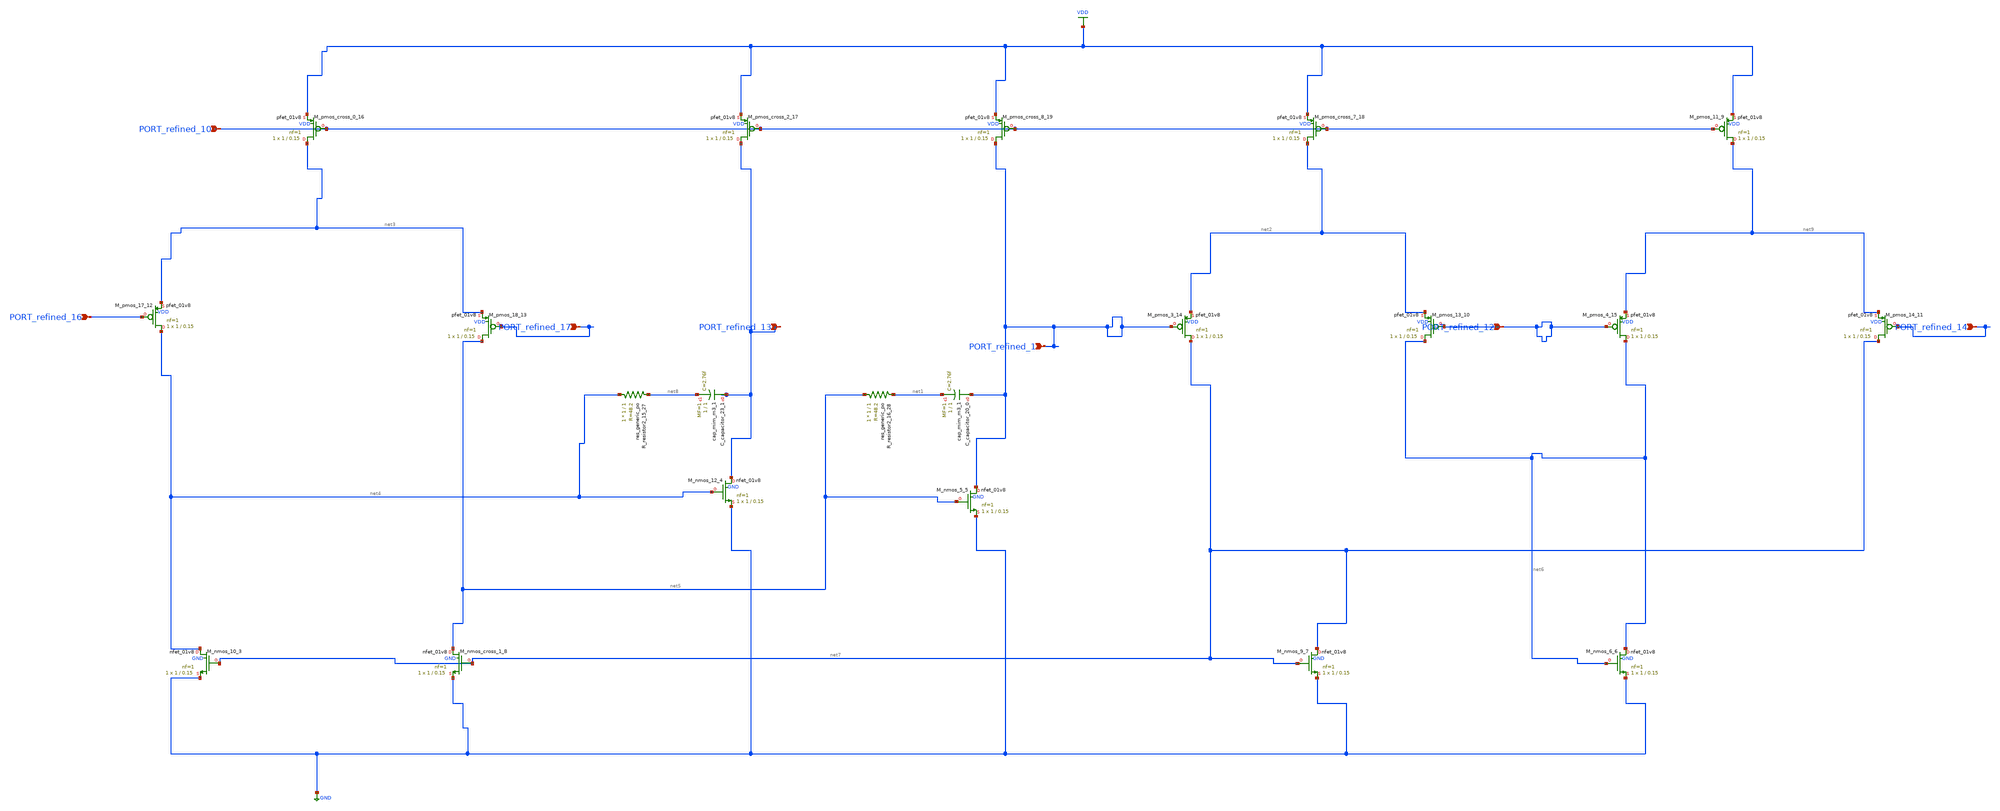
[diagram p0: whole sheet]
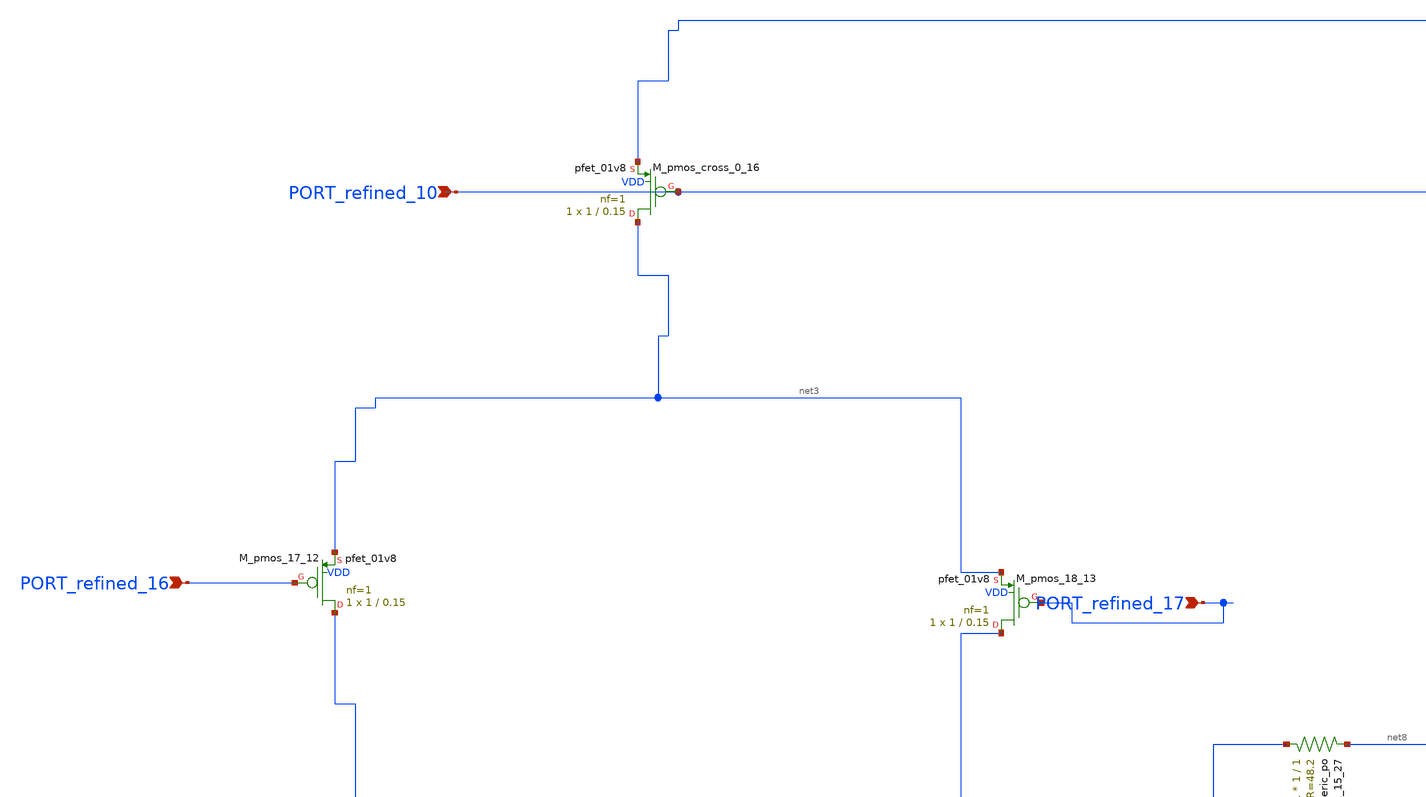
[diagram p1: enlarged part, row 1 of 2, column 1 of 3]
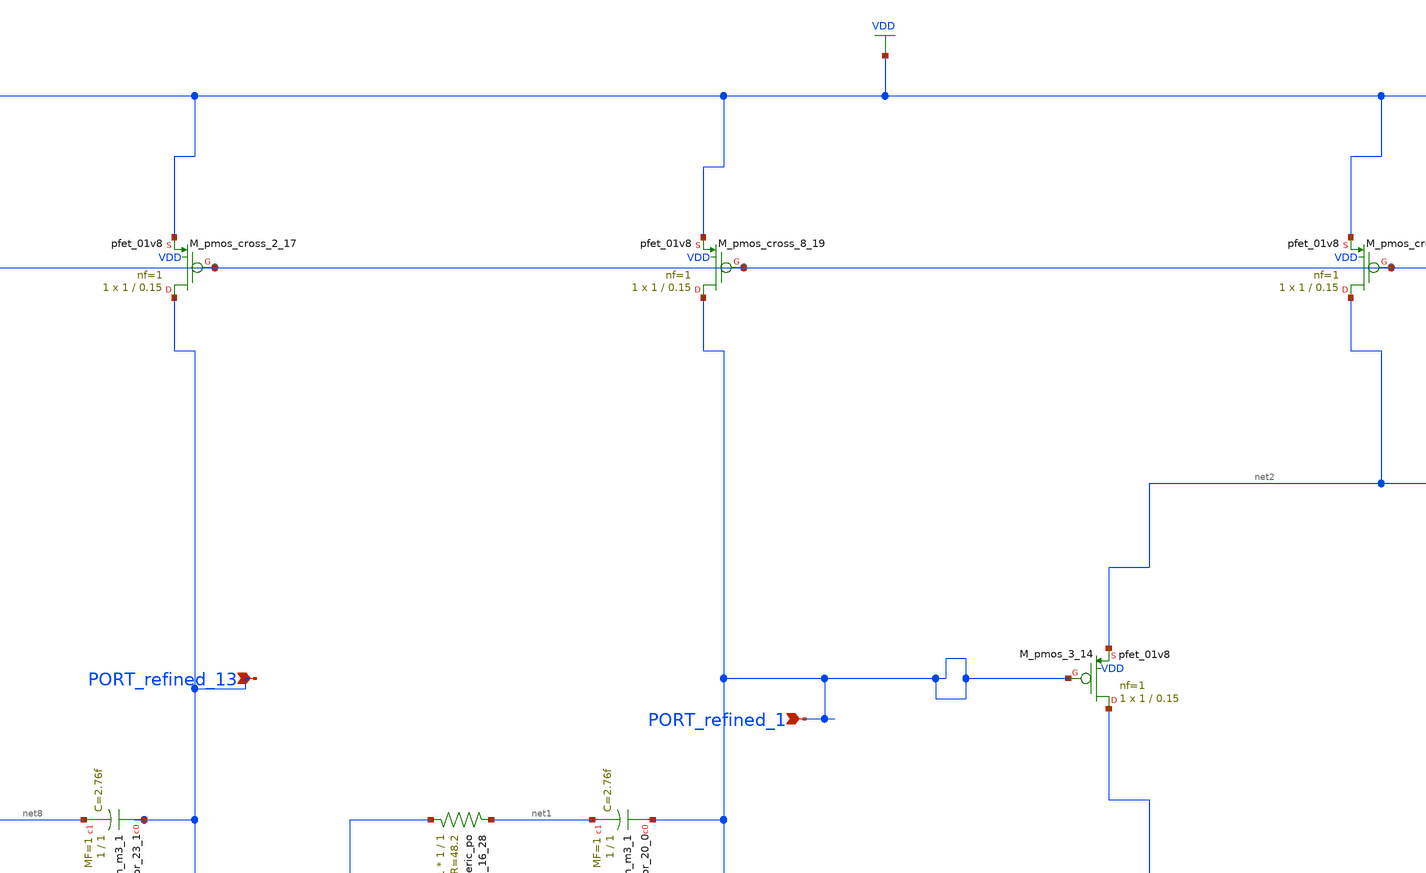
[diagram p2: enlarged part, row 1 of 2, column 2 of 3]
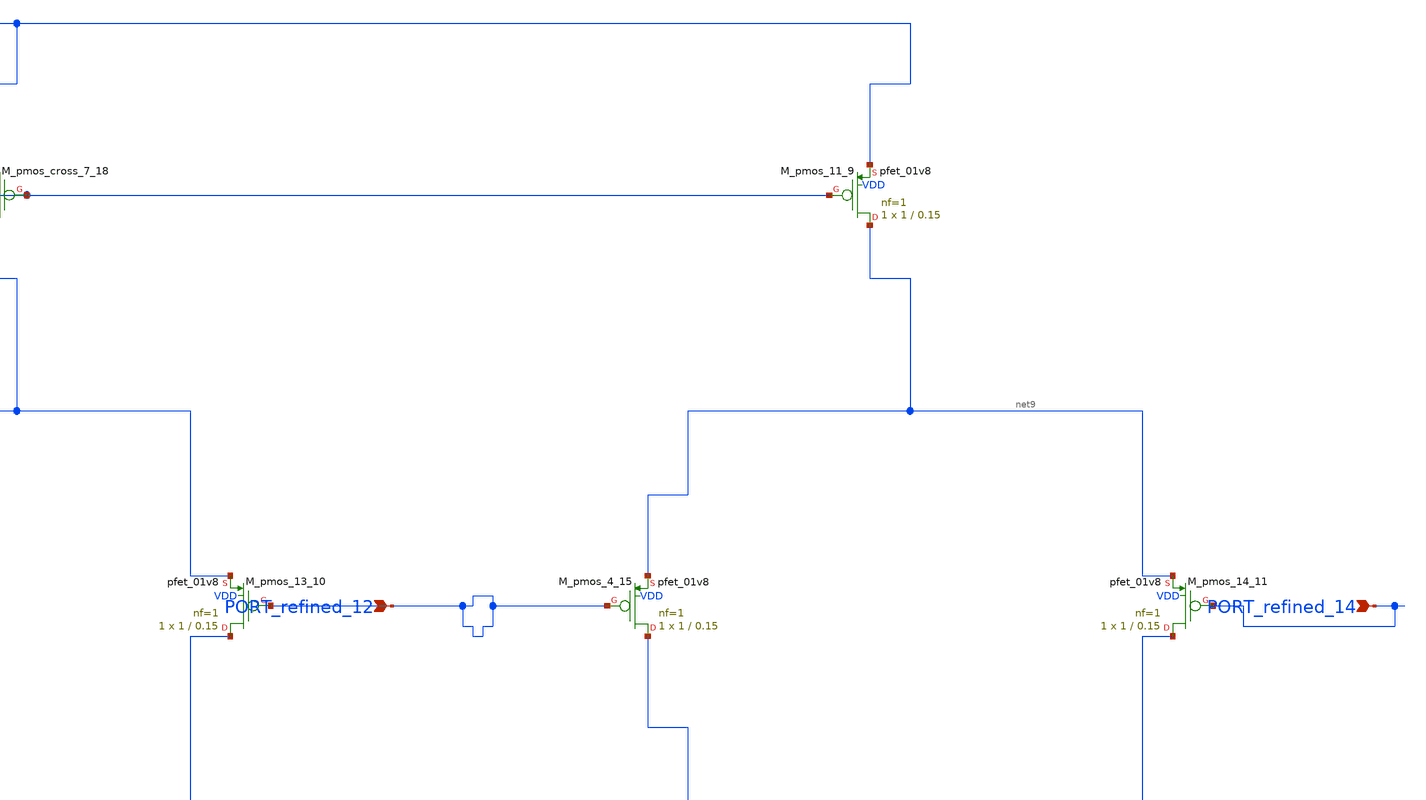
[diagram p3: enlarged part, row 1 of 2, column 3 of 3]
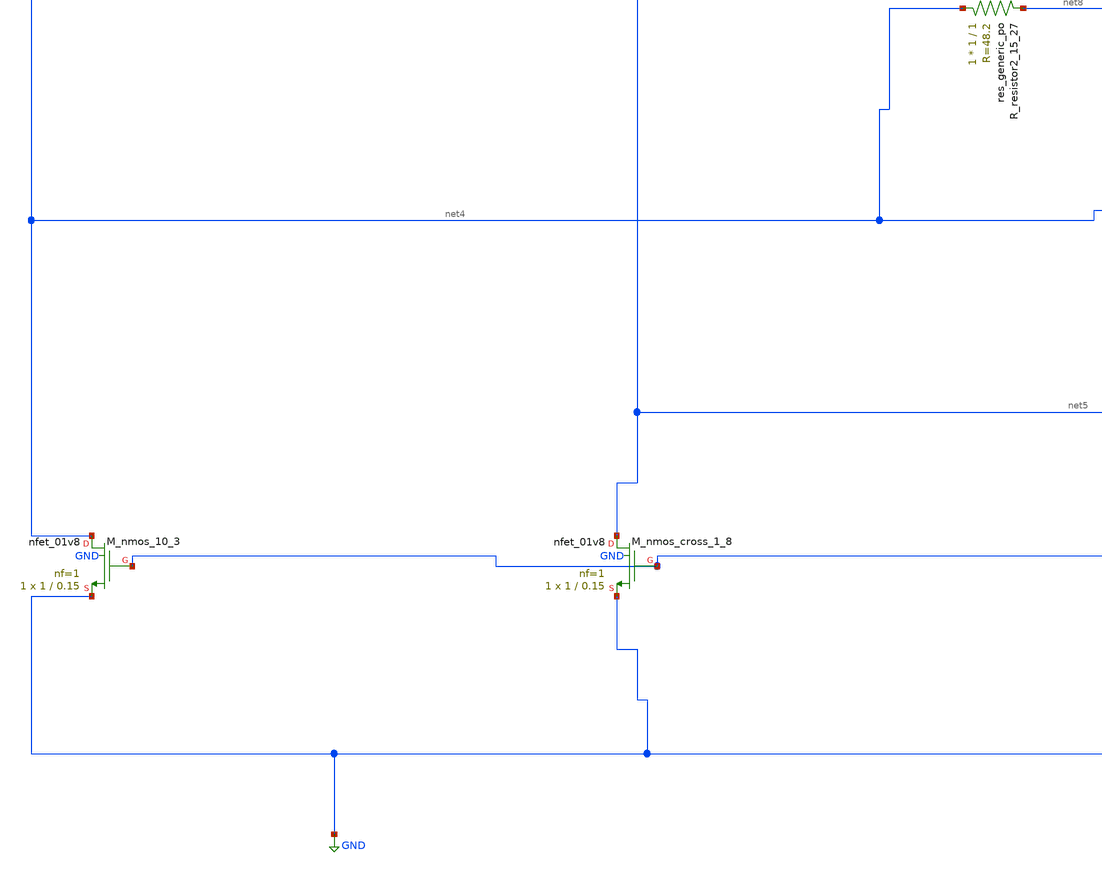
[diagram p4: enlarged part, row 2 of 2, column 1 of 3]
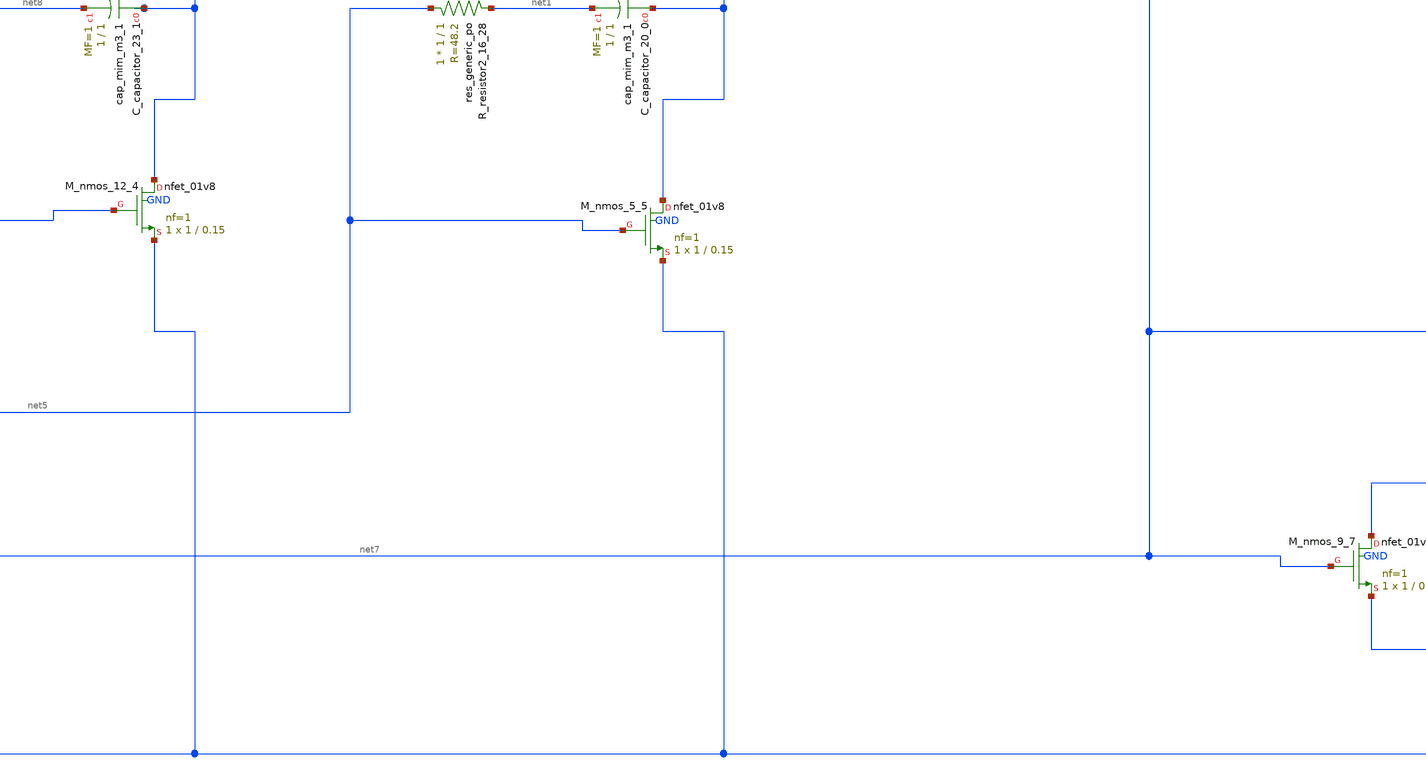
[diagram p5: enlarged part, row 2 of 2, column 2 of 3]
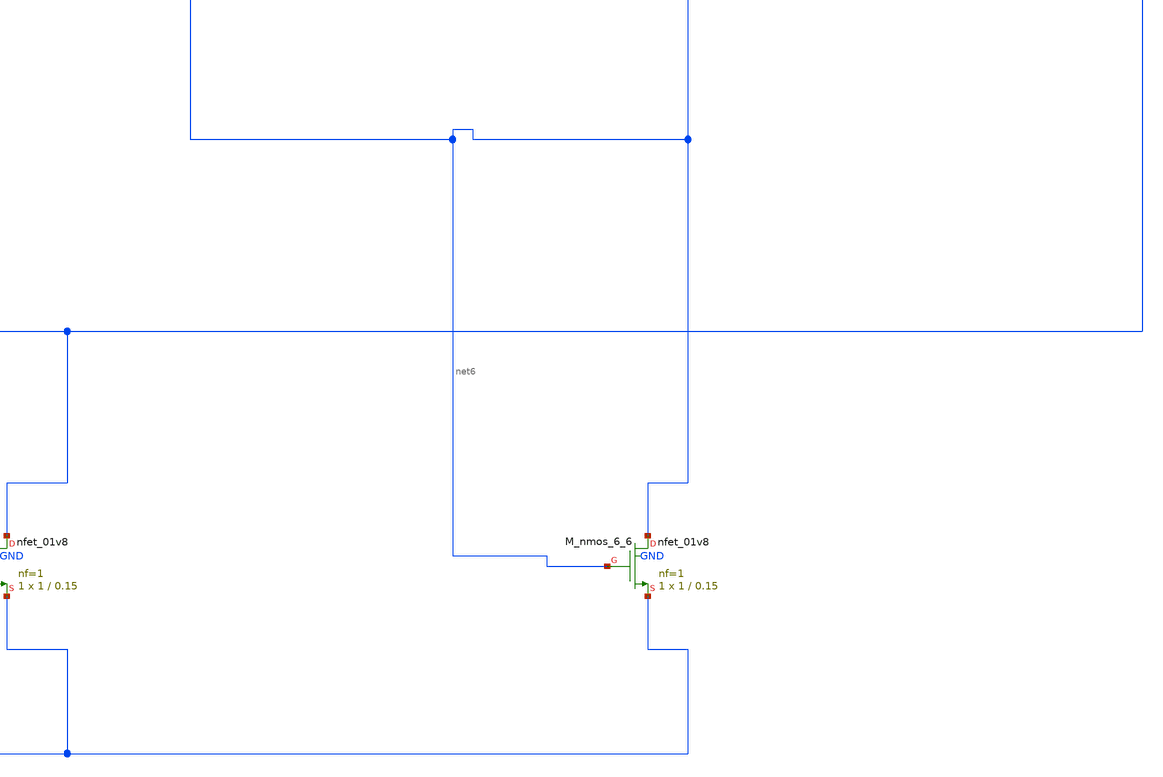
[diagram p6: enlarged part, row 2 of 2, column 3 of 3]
** sch_path: schematics/SchemGen/10_1109_ACCESS_2021_3087737_04_003.sch
**.subckt 10_1109_ACCESS_2021_3087737_04_003 PORT_refined_10 PORT_refined_13 PORT_refined_16
*+ PORT_refined_17 PORT_refined_1 PORT_refined_12 PORT_refined_14
*.ipin PORT_refined_10
*.ipin PORT_refined_13
*.ipin PORT_refined_16
*.ipin PORT_refined_17
*.ipin PORT_refined_1
*.ipin PORT_refined_12
*.ipin PORT_refined_14
XC_capacitor_20_0 PORT_refined_1 net1 sky130_fd_pr__cap_mim_m3_1 W=1 L=1 MF=1 m=1
XC_capacitor_23_1 PORT_refined_13 net8 sky130_fd_pr__cap_mim_m3_1 W=1 L=1 MF=1 m=1
XM_nmos_10_3 net4 net7 GND GND sky130_fd_pr__nfet_01v8 L=0.15 W=1 nf=1 ad='int((1 + 1)/2) * 1 / 1 * 0.29'
+ as='int((1 + 2)/2) * 1 / 1 * 0.29' pd='2*int((1 + 1)/2) * (1 / 1 + 0.29)' ps='2*int((1 + 2)/2) * (1 / 1 + 0.29)'
+ nrd='0.29 / 1 ' nrs='0.29 / 1 ' sa=0 sb=0 sd=0 mult=1 m=1
XM_nmos_12_4 PORT_refined_13 net4 GND GND sky130_fd_pr__nfet_01v8 L=0.15 W=1 nf=1 ad='int((1 + 1)/2) * 1 / 1 * 0.29'
+ as='int((1 + 2)/2) * 1 / 1 * 0.29' pd='2*int((1 + 1)/2) * (1 / 1 + 0.29)' ps='2*int((1 + 2)/2) * (1 / 1 + 0.29)'
+ nrd='0.29 / 1 ' nrs='0.29 / 1 ' sa=0 sb=0 sd=0 mult=1 m=1
XM_nmos_5_5 PORT_refined_1 net5 GND GND sky130_fd_pr__nfet_01v8 L=0.15 W=1 nf=1 ad='int((1 + 1)/2) * 1 / 1 * 0.29'
+ as='int((1 + 2)/2) * 1 / 1 * 0.29' pd='2*int((1 + 1)/2) * (1 / 1 + 0.29)' ps='2*int((1 + 2)/2) * (1 / 1 + 0.29)'
+ nrd='0.29 / 1 ' nrs='0.29 / 1 ' sa=0 sb=0 sd=0 mult=1 m=1
XM_nmos_6_6 net6 net6 GND GND sky130_fd_pr__nfet_01v8 L=0.15 W=1 nf=1 ad='int((1 + 1)/2) * 1 / 1 * 0.29'
+ as='int((1 + 2)/2) * 1 / 1 * 0.29' pd='2*int((1 + 1)/2) * (1 / 1 + 0.29)' ps='2*int((1 + 2)/2) * (1 / 1 + 0.29)'
+ nrd='0.29 / 1 ' nrs='0.29 / 1 ' sa=0 sb=0 sd=0 mult=1 m=1
XM_nmos_9_7 net7 net7 GND GND sky130_fd_pr__nfet_01v8 L=0.15 W=1 nf=1 ad='int((1 + 1)/2) * 1 / 1 * 0.29'
+ as='int((1 + 2)/2) * 1 / 1 * 0.29' pd='2*int((1 + 1)/2) * (1 / 1 + 0.29)' ps='2*int((1 + 2)/2) * (1 / 1 + 0.29)'
+ nrd='0.29 / 1 ' nrs='0.29 / 1 ' sa=0 sb=0 sd=0 mult=1 m=1
XM_nmos_cross_1_8 net5 net7 GND GND sky130_fd_pr__nfet_01v8 L=0.15 W=1 nf=1 ad='int((1 + 1)/2) * 1 / 1 * 0.29'
+ as='int((1 + 2)/2) * 1 / 1 * 0.29' pd='2*int((1 + 1)/2) * (1 / 1 + 0.29)' ps='2*int((1 + 2)/2) * (1 / 1 + 0.29)'
+ nrd='0.29 / 1 ' nrs='0.29 / 1 ' sa=0 sb=0 sd=0 mult=1 m=1
XM_pmos_11_9 net9 PORT_refined_10 VDD VDD sky130_fd_pr__pfet_01v8 L=0.15 W=1 nf=1 ad='int((1 + 1)/2) * 1 / 1 * 0.29'
+ as='int((1 + 2)/2) * 1 / 1 * 0.29' pd='2*int((1 + 1)/2) * (1 / 1 + 0.29)' ps='2*int((1 + 2)/2) * (1 / 1 + 0.29)'
+ nrd='0.29 / 1 ' nrs='0.29 / 1 ' sa=0 sb=0 sd=0 mult=1 m=1
XM_pmos_13_10 net6 PORT_refined_12 net2 VDD sky130_fd_pr__pfet_01v8 L=0.15 W=1 nf=1 ad='int((1 + 1)/2) * 1 / 1 * 0.29'
+ as='int((1 + 2)/2) * 1 / 1 * 0.29' pd='2*int((1 + 1)/2) * (1 / 1 + 0.29)' ps='2*int((1 + 2)/2) * (1 / 1 + 0.29)'
+ nrd='0.29 / 1 ' nrs='0.29 / 1 ' sa=0 sb=0 sd=0 mult=1 m=1
XM_pmos_14_11 net7 PORT_refined_14 net9 VDD sky130_fd_pr__pfet_01v8 L=0.15 W=1 nf=1 ad='int((1 + 1)/2) * 1 / 1 * 0.29'
+ as='int((1 + 2)/2) * 1 / 1 * 0.29' pd='2*int((1 + 1)/2) * (1 / 1 + 0.29)' ps='2*int((1 + 2)/2) * (1 / 1 + 0.29)'
+ nrd='0.29 / 1 ' nrs='0.29 / 1 ' sa=0 sb=0 sd=0 mult=1 m=1
XM_pmos_17_12 net4 PORT_refined_16 net3 VDD sky130_fd_pr__pfet_01v8 L=0.15 W=1 nf=1 ad='int((1 + 1)/2) * 1 / 1 * 0.29'
+ as='int((1 + 2)/2) * 1 / 1 * 0.29' pd='2*int((1 + 1)/2) * (1 / 1 + 0.29)' ps='2*int((1 + 2)/2) * (1 / 1 + 0.29)'
+ nrd='0.29 / 1 ' nrs='0.29 / 1 ' sa=0 sb=0 sd=0 mult=1 m=1
XM_pmos_18_13 net5 PORT_refined_17 net3 VDD sky130_fd_pr__pfet_01v8 L=0.15 W=1 nf=1 ad='int((1 + 1)/2) * 1 / 1 * 0.29'
+ as='int((1 + 2)/2) * 1 / 1 * 0.29' pd='2*int((1 + 1)/2) * (1 / 1 + 0.29)' ps='2*int((1 + 2)/2) * (1 / 1 + 0.29)'
+ nrd='0.29 / 1 ' nrs='0.29 / 1 ' sa=0 sb=0 sd=0 mult=1 m=1
XM_pmos_3_14 net7 PORT_refined_1 net2 VDD sky130_fd_pr__pfet_01v8 L=0.15 W=1 nf=1 ad='int((1 + 1)/2) * 1 / 1 * 0.29'
+ as='int((1 + 2)/2) * 1 / 1 * 0.29' pd='2*int((1 + 1)/2) * (1 / 1 + 0.29)' ps='2*int((1 + 2)/2) * (1 / 1 + 0.29)'
+ nrd='0.29 / 1 ' nrs='0.29 / 1 ' sa=0 sb=0 sd=0 mult=1 m=1
XM_pmos_4_15 net6 PORT_refined_12 net9 VDD sky130_fd_pr__pfet_01v8 L=0.15 W=1 nf=1 ad='int((1 + 1)/2) * 1 / 1 * 0.29'
+ as='int((1 + 2)/2) * 1 / 1 * 0.29' pd='2*int((1 + 1)/2) * (1 / 1 + 0.29)' ps='2*int((1 + 2)/2) * (1 / 1 + 0.29)'
+ nrd='0.29 / 1 ' nrs='0.29 / 1 ' sa=0 sb=0 sd=0 mult=1 m=1
XM_pmos_cross_0_16 net3 PORT_refined_10 VDD VDD sky130_fd_pr__pfet_01v8 L=0.15 W=1 nf=1 ad='int((1 + 1)/2) * 1 / 1 * 0.29'
+ as='int((1 + 2)/2) * 1 / 1 * 0.29' pd='2*int((1 + 1)/2) * (1 / 1 + 0.29)' ps='2*int((1 + 2)/2) * (1 / 1 + 0.29)'
+ nrd='0.29 / 1 ' nrs='0.29 / 1 ' sa=0 sb=0 sd=0 mult=1 m=1
XM_pmos_cross_2_17 PORT_refined_13 PORT_refined_10 VDD VDD sky130_fd_pr__pfet_01v8 L=0.15 W=1 nf=1 ad='int((1 + 1)/2) * 1 / 1 * 0.29'
+ as='int((1 + 2)/2) * 1 / 1 * 0.29' pd='2*int((1 + 1)/2) * (1 / 1 + 0.29)' ps='2*int((1 + 2)/2) * (1 / 1 + 0.29)'
+ nrd='0.29 / 1 ' nrs='0.29 / 1 ' sa=0 sb=0 sd=0 mult=1 m=1
XM_pmos_cross_7_18 net2 PORT_refined_10 VDD VDD sky130_fd_pr__pfet_01v8 L=0.15 W=1 nf=1 ad='int((1 + 1)/2) * 1 / 1 * 0.29'
+ as='int((1 + 2)/2) * 1 / 1 * 0.29' pd='2*int((1 + 1)/2) * (1 / 1 + 0.29)' ps='2*int((1 + 2)/2) * (1 / 1 + 0.29)'
+ nrd='0.29 / 1 ' nrs='0.29 / 1 ' sa=0 sb=0 sd=0 mult=1 m=1
XM_pmos_cross_8_19 PORT_refined_1 PORT_refined_10 VDD VDD sky130_fd_pr__pfet_01v8 L=0.15 W=1 nf=1 ad='int((1 + 1)/2) * 1 / 1 * 0.29'
+ as='int((1 + 2)/2) * 1 / 1 * 0.29' pd='2*int((1 + 1)/2) * (1 / 1 + 0.29)' ps='2*int((1 + 2)/2) * (1 / 1 + 0.29)'
+ nrd='0.29 / 1 ' nrs='0.29 / 1 ' sa=0 sb=0 sd=0 mult=1 m=1
XR_resistor2_15_27 net4 net8 sky130_fd_pr__res_generic_po W=1 L=1 m=1
XR_resistor2_16_28 net5 net1 sky130_fd_pr__res_generic_po W=1 L=1 m=1
**.ends
.GLOBAL GND
.GLOBAL VDD
.end
